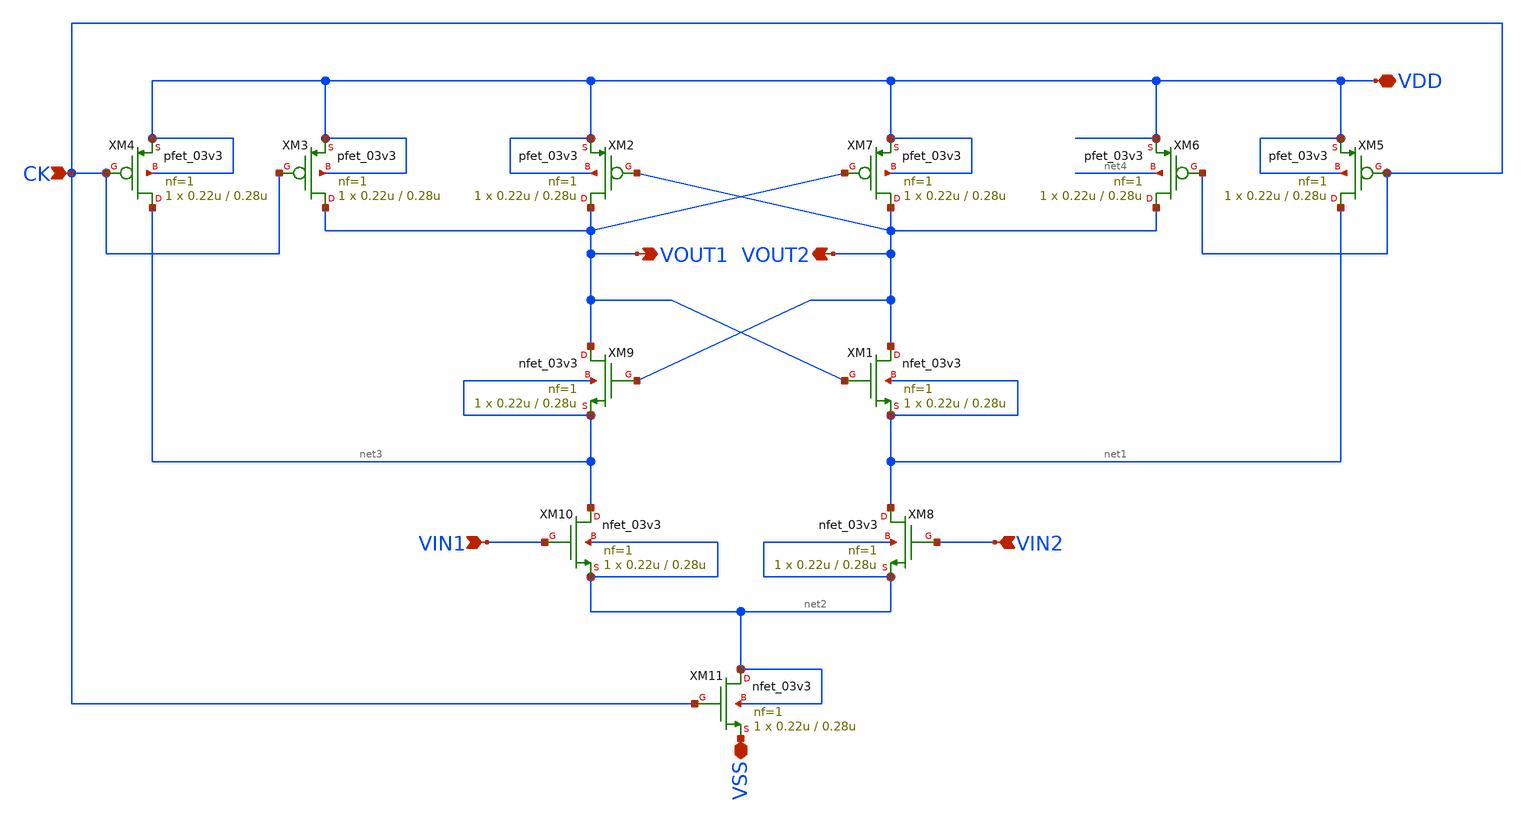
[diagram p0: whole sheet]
** sch_path: comparator/schematic/backup_files/strongarm copy.sch
**.subckt strongarm copy VOUT1 VOUT2 VIN1 VIN2 CK VDD VSS
*.opin VOUT1
*.opin VOUT2
*.ipin VIN1
*.ipin VIN2
*.ipin CK
*.iopin VDD
*.iopin VSS
XM1 VOUT2 VOUT1 net1 net1 nfet_03v3 L=0.28u W=0.22u nf=1 ad='int((nf+1)/2) * W/nf * 0.18u' as='int((nf+2)/2) * W/nf * 0.18u'
+ pd='2*int((nf+1)/2) * (W/nf + 0.18u)' ps='2*int((nf+2)/2) * (W/nf + 0.18u)' nrd='0.18u / W' nrs='0.18u / W'
+ sa=0 sb=0 sd=0 m=1
XM2 VOUT1 VOUT2 VDD VDD pfet_03v3 L=0.28u W=0.22u nf=1 ad='int((nf+1)/2) * W/nf * 0.18u' as='int((nf+2)/2) * W/nf * 0.18u'
+ pd='2*int((nf+1)/2) * (W/nf + 0.18u)' ps='2*int((nf+2)/2) * (W/nf + 0.18u)' nrd='0.18u / W' nrs='0.18u / W'
+ sa=0 sb=0 sd=0 m=1
XM3 VOUT1 CK VDD VDD pfet_03v3 L=0.28u W=0.22u nf=1 ad='int((nf+1)/2) * W/nf * 0.18u' as='int((nf+2)/2) * W/nf * 0.18u'
+ pd='2*int((nf+1)/2) * (W/nf + 0.18u)' ps='2*int((nf+2)/2) * (W/nf + 0.18u)' nrd='0.18u / W' nrs='0.18u / W'
+ sa=0 sb=0 sd=0 m=1
XM4 net3 CK VDD VDD pfet_03v3 L=0.28u W=0.22u nf=1 ad='int((nf+1)/2) * W/nf * 0.18u' as='int((nf+2)/2) * W/nf * 0.18u'
+ pd='2*int((nf+1)/2) * (W/nf + 0.18u)' ps='2*int((nf+2)/2) * (W/nf + 0.18u)' nrd='0.18u / W' nrs='0.18u / W'
+ sa=0 sb=0 sd=0 m=1
XM5 net1 CK VDD VDD pfet_03v3 L=0.28u W=0.22u nf=1 ad='int((nf+1)/2) * W/nf * 0.18u' as='int((nf+2)/2) * W/nf * 0.18u'
+ pd='2*int((nf+1)/2) * (W/nf + 0.18u)' ps='2*int((nf+2)/2) * (W/nf + 0.18u)' nrd='0.18u / W' nrs='0.18u / W'
+ sa=0 sb=0 sd=0 m=1
XM6 VOUT2 CK VDD net4 pfet_03v3 L=0.28u W=0.22u nf=1 ad='int((nf+1)/2) * W/nf * 0.18u' as='int((nf+2)/2) * W/nf * 0.18u'
+ pd='2*int((nf+1)/2) * (W/nf + 0.18u)' ps='2*int((nf+2)/2) * (W/nf + 0.18u)' nrd='0.18u / W' nrs='0.18u / W'
+ sa=0 sb=0 sd=0 m=1
XM7 VOUT2 VOUT1 VDD VDD pfet_03v3 L=0.28u W=0.22u nf=1 ad='int((nf+1)/2) * W/nf * 0.18u' as='int((nf+2)/2) * W/nf * 0.18u'
+ pd='2*int((nf+1)/2) * (W/nf + 0.18u)' ps='2*int((nf+2)/2) * (W/nf + 0.18u)' nrd='0.18u / W' nrs='0.18u / W'
+ sa=0 sb=0 sd=0 m=1
XM8 net1 VIN2 net2 net2 nfet_03v3 L=0.28u W=0.22u nf=1 ad='int((nf+1)/2) * W/nf * 0.18u' as='int((nf+2)/2) * W/nf * 0.18u'
+ pd='2*int((nf+1)/2) * (W/nf + 0.18u)' ps='2*int((nf+2)/2) * (W/nf + 0.18u)' nrd='0.18u / W' nrs='0.18u / W'
+ sa=0 sb=0 sd=0 m=1
XM9 VOUT1 VOUT2 net3 net3 nfet_03v3 L=0.28u W=0.22u nf=1 ad='int((nf+1)/2) * W/nf * 0.18u' as='int((nf+2)/2) * W/nf * 0.18u'
+ pd='2*int((nf+1)/2) * (W/nf + 0.18u)' ps='2*int((nf+2)/2) * (W/nf + 0.18u)' nrd='0.18u / W' nrs='0.18u / W'
+ sa=0 sb=0 sd=0 m=1
XM10 net3 VIN1 net2 net2 nfet_03v3 L=0.28u W=0.22u nf=1 ad='int((nf+1)/2) * W/nf * 0.18u' as='int((nf+2)/2) * W/nf * 0.18u'
+ pd='2*int((nf+1)/2) * (W/nf + 0.18u)' ps='2*int((nf+2)/2) * (W/nf + 0.18u)' nrd='0.18u / W' nrs='0.18u / W'
+ sa=0 sb=0 sd=0 m=1
XM11 net2 CK VSS net2 nfet_03v3 L=0.28u W=0.22u nf=1 ad='int((nf+1)/2) * W/nf * 0.18u' as='int((nf+2)/2) * W/nf * 0.18u'
+ pd='2*int((nf+1)/2) * (W/nf + 0.18u)' ps='2*int((nf+2)/2) * (W/nf + 0.18u)' nrd='0.18u / W' nrs='0.18u / W'
+ sa=0 sb=0 sd=0 m=1
**.ends
.end
